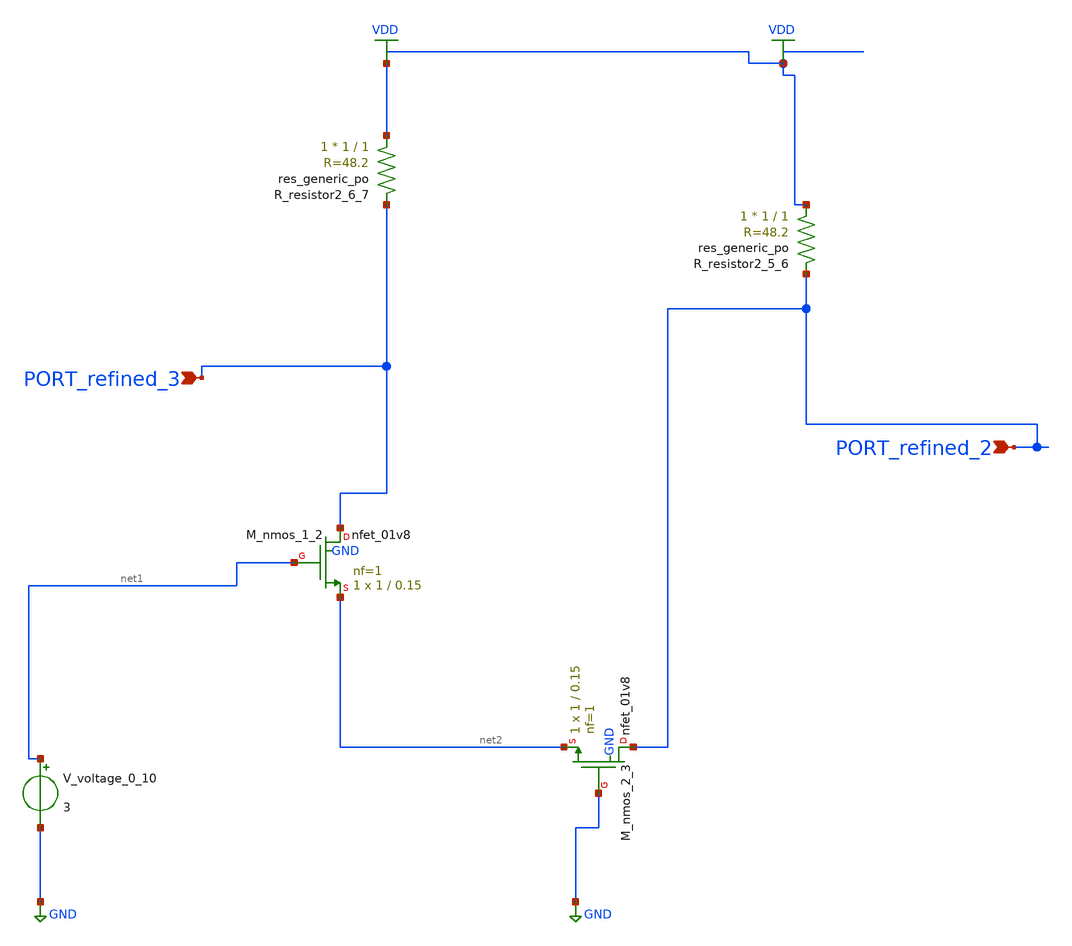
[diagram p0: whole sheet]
** sch_path: schematics/AMSNet/197.sch
**.subckt 197 PORT_refined_3 PORT_refined_2
*.ipin PORT_refined_3
*.ipin PORT_refined_2
XM_nmos_1_2 PORT_refined_3 net1 net2 GND sky130_fd_pr__nfet_01v8 L=0.15 W=1 nf=1 ad='int((1 + 1)/2) * 1 / 1 * 0.29'
+ as='int((1 + 2)/2) * 1 / 1 * 0.29' pd='2*int((1 + 1)/2) * (1 / 1 + 0.29)' ps='2*int((1 + 2)/2) * (1 / 1 + 0.29)'
+ nrd='0.29 / 1 ' nrs='0.29 / 1 ' sa=0 sb=0 sd=0 mult=1 m=1
XM_nmos_2_3 PORT_refined_2 GND net2 GND sky130_fd_pr__nfet_01v8 L=0.15 W=1 nf=1 ad='int((1 + 1)/2) * 1 / 1 * 0.29'
+ as='int((1 + 2)/2) * 1 / 1 * 0.29' pd='2*int((1 + 1)/2) * (1 / 1 + 0.29)' ps='2*int((1 + 2)/2) * (1 / 1 + 0.29)'
+ nrd='0.29 / 1 ' nrs='0.29 / 1 ' sa=0 sb=0 sd=0 mult=1 m=1
XR_resistor2_5_6 VDD PORT_refined_2 sky130_fd_pr__res_generic_po W=1 L=1 m=1
XR_resistor2_6_7 VDD PORT_refined_3 sky130_fd_pr__res_generic_po W=1 L=1 m=1
V_voltage_0_10 net1 GND 3
**.ends
.GLOBAL GND
.GLOBAL VDD
.end
